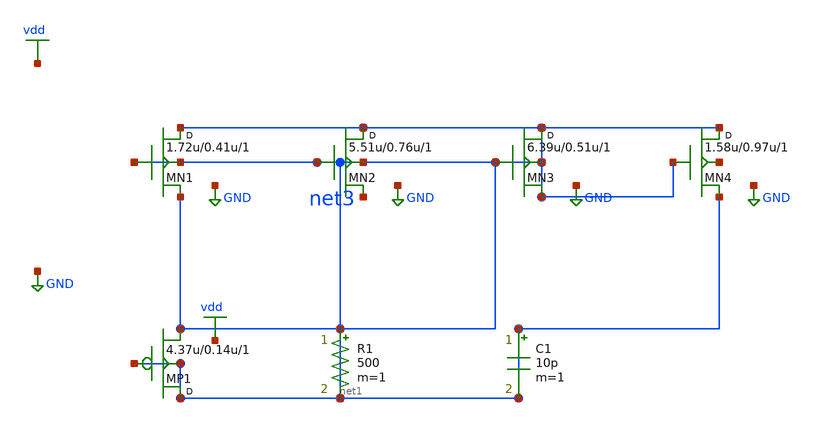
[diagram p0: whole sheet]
** sch_path: synthetic/generated/0040_synthetic.sch
**.subckt 0040_synthetic
MN1 net1 net1 net1 net1 nmos w=1.72u l=0.41u m=1
MN2 net1 net1 net3 net1 nmos w=5.51u l=0.76u m=1
MN3 net1 net1 net1 net1 nmos w=6.39u l=0.51u m=1
MN4 net1 net1 net1 net2 nmos w=1.58u l=0.97u m=1
MP1 net1 net1 net1 net1 pmos w=4.37u l=0.14u m=1
R1 net1 net1 500 m=1
C1 net1 net1 10p m=1
**.ends
.GLOBAL GND
.GLOBAL vdd
.end
